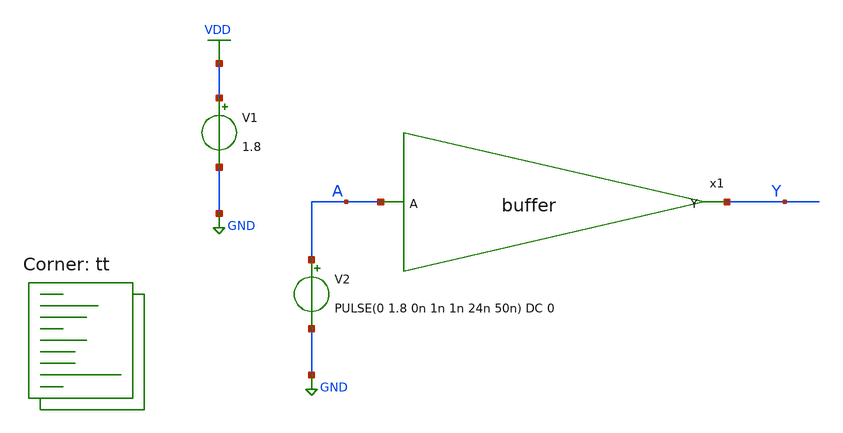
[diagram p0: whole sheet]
** sch_path: eng331lab_final/eng331lab_xschem/tb_buffer_h.sch
**.subckt tb_buffer_h
V1 VDD GND 1.8
V2 A GND PULSE(0 1.8 0n 1n 1n 24n 50n) DC 0
x1 Y A buffer
**** begin user architecture code
.lib $::SKYWATER_MODELS/sky130.lib.spice tt

.control
  save all
  tran 10n 400n
  write tb_buffer_h.raw
  set appendwrite
.endc


**** end user architecture code
**.ends

* expanding   symbol:  eng331lab_xschem/buffer.sym # of pins=2
** sym_path: eng331lab_final/eng331lab_xschem/buffer.sym
** sch_path: eng331lab_final/eng331lab_xschem/buffer.sch
.subckt buffer Y A
*.ipin A
*.opin Y
x1 Y_bar A inv
x2 Y Y_bar inv
.ends


* expanding   symbol:  /home/student/xschem_sky130/eng331lab_xschem/inv.sym # of pins=2
** sym_path: eng331lab_final/eng331lab_xschem/inv.sym
** sch_path: eng331lab_final/eng331lab_xschem/inv.sch
.subckt inv Y A
*.ipin A
*.opin Y
XM1 Y A VDD VDD sky130_fd_pr__pfet_01v8 L=0.15 W=0.8 nf=1 ad='int((1 + 1)/2) * 0.8 / 1 * 0.29' as='int((1 + 2)/2) * 0.8 / 1 * 0.29'
+ pd='2*int((1 + 1)/2) * (0.8 / 1 + 0.29)' ps='2*int((1 + 2)/2) * (0.8 / 1 + 0.29)' nrd='0.29 / 0.8 ' nrs='0.29 / 0.8 '
+ sa=0 sb=0 sd=0 mult=1 m=1
XM2 Y A GND GND sky130_fd_pr__nfet_01v8 L=0.15 W=0.5 nf=1 ad='int((1 + 1)/2) * 0.5 / 1 * 0.29' as='int((1 + 2)/2) * 0.5 / 1 * 0.29'
+ pd='2*int((1 + 1)/2) * (0.5 / 1 + 0.29)' ps='2*int((1 + 2)/2) * (0.5 / 1 + 0.29)' nrd='0.29 / 0.5 ' nrs='0.29 / 0.5 '
+ sa=0 sb=0 sd=0 mult=1 m=1
.ends

.GLOBAL VDD
.GLOBAL GND
.end
